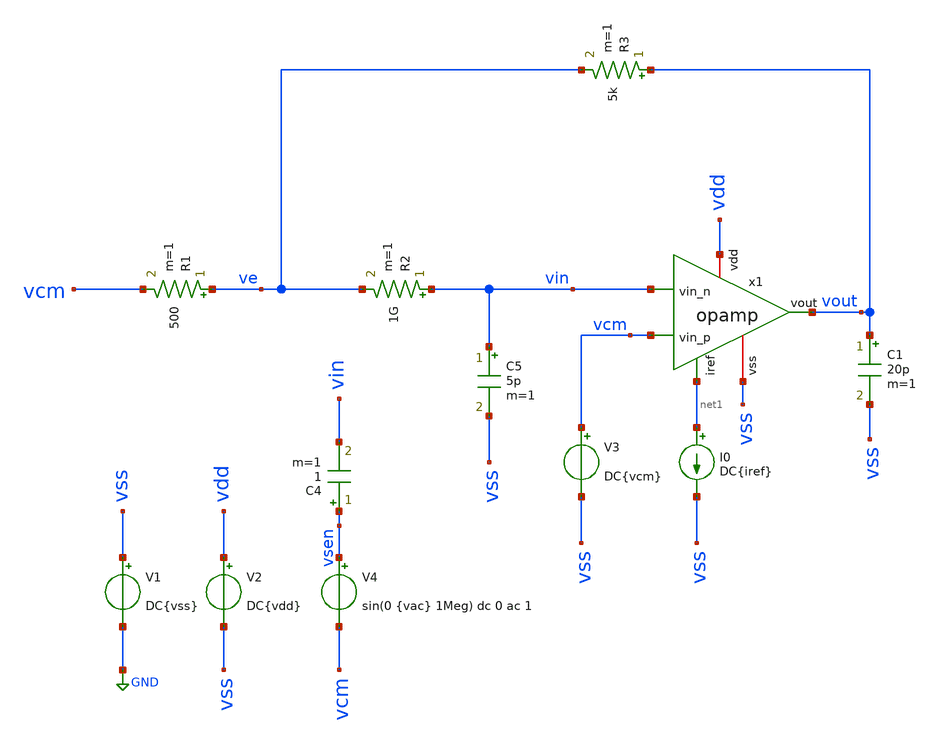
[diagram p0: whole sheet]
** sch_path: xsch/sch/opamp/opamp_openloop.sch
**.subckt opamp_openloop
V1 vss GND DC{vss}
V2 vdd vss DC{vdd}
V3 vcm vss DC{vcm}
V4 vsen vcm sin(0 {vac} 1Meg) dc 0 ac 1
C4 vsen vin 1 m=1
I0 net1 vss DC{iref}
R1 ve vcm 500 m=1
R2 vin ve 1G m=1
R3 vout ve 5k m=1
C5 vin vss 5p m=1
C1 vout vss 20p m=1
x1 vdd net1 vin vcm vout vss opamp
**** begin user architecture code




* Circuit Parameters
.param iref = 100u
.param vdd  = 1.8
.param vss  = 0.0
.param vcm  = 0.8
.param vac  = 10m
.options TEMP = 65.0

* Include Models
.lib /home/tools/repos_sky130/skywater-pdk/libraries/sky130_fd_pr_ngspice/latest/models/corners/sky130.lib FS

* OP Parameters & Singals to save
.save all  @M.X1.XM1.msky130_fd_pr__pfet_01v8[id] @M.X1.XM1.msky130_fd_pr__pfet_01v8[vth] @M.X1.XM1.msky130_fd_pr__pfet_01v8[vgs] @M.X1.XM1.msky130_fd_pr__pfet_01v8[vds] @M.X1.XM1.msky130_fd_pr__pfet_01v8[vdsat] @M.X1.XM1.msky130_fd_pr__pfet_01v8[gm] @M.X1.XM1.msky130_fd_pr__pfet_01v8[gds]  @M.X1.XM2.msky130_fd_pr__pfet_01v8[id] @M.X1.XM2.msky130_fd_pr__pfet_01v8[vth] @M.X1.XM2.msky130_fd_pr__pfet_01v8[vgs] @M.X1.XM2.msky130_fd_pr__pfet_01v8[vds] @M.X1.XM2.msky130_fd_pr__pfet_01v8[vdsat] @M.X1.XM2.msky130_fd_pr__pfet_01v8[gm] @M.X1.XM2.msky130_fd_pr__pfet_01v8[gds]  @M.X1.XM3.msky130_fd_pr__nfet_01v8[id] @M.X1.XM3.msky130_fd_pr__nfet_01v8[vth] @M.X1.XM3.msky130_fd_pr__nfet_01v8[vgs] @M.X1.XM3.msky130_fd_pr__nfet_01v8[vds] @M.X1.XM3.msky130_fd_pr__nfet_01v8[vdsat] @M.X1.XM3.msky130_fd_pr__nfet_01v8[gm] @M.X1.XM3.msky130_fd_pr__nfet_01v8[gds]  @M.X1.XM4.msky130_fd_pr__nfet_01v8[id] @M.X1.XM4.msky130_fd_pr__nfet_01v8[vth] @M.X1.XM4.msky130_fd_pr__nfet_01v8[vgs] @M.X1.XM4.msky130_fd_pr__nfet_01v8[vds] @M.X1.XM4.msky130_fd_pr__nfet_01v8[vdsat] @M.X1.XM4.msky130_fd_pr__nfet_01v8[gm] @M.X1.XM4.msky130_fd_pr__nfet_01v8[gds]  @M.X1.XM5.msky130_fd_pr__pfet_01v8[id] @M.X1.XM5.msky130_fd_pr__pfet_01v8[vth] @M.X1.XM5.msky130_fd_pr__pfet_01v8[vgs] @M.X1.XM5.msky130_fd_pr__pfet_01v8[vds] @M.X1.XM5.msky130_fd_pr__pfet_01v8[vdsat] @M.X1.XM5.msky130_fd_pr__pfet_01v8[gm] @M.X1.XM5.msky130_fd_pr__pfet_01v8[gds]  @M.X1.XM6.msky130_fd_pr__nfet_01v8[id] @M.X1.XM6.msky130_fd_pr__nfet_01v8[vth] @M.X1.XM6.msky130_fd_pr__nfet_01v8[vgs] @M.X1.XM6.msky130_fd_pr__nfet_01v8[vds] @M.X1.XM6.msky130_fd_pr__nfet_01v8[vdsat] @M.X1.XM6.msky130_fd_pr__nfet_01v8[gm] @M.X1.XM6.msky130_fd_pr__nfet_01v8[gds]  @M.X1.XM7.msky130_fd_pr__pfet_01v8[id] @M.X1.XM7.msky130_fd_pr__pfet_01v8[vth] @M.X1.XM7.msky130_fd_pr__pfet_01v8[vgs] @M.X1.XM7.msky130_fd_pr__pfet_01v8[vds] @M.X1.XM7.msky130_fd_pr__pfet_01v8[vdsat] @M.X1.XM7.msky130_fd_pr__pfet_01v8[gm] @M.X1.XM7.msky130_fd_pr__pfet_01v8[gds]  @M.X1.XM8.msky130_fd_pr__pfet_01v8[id] @M.X1.XM8.msky130_fd_pr__pfet_01v8[vth] @M.X1.XM8.msky130_fd_pr__pfet_01v8[vgs] @M.X1.XM8.msky130_fd_pr__pfet_01v8[vds] @M.X1.XM8.msky130_fd_pr__pfet_01v8[vdsat] @M.X1.XM8.msky130_fd_pr__pfet_01v8[gm] @M.X1.XM8.msky130_fd_pr__pfet_01v8[gds]  @M.X1.XM9.msky130_fd_pr__nfet_01v8[id] @M.X1.XM9.msky130_fd_pr__nfet_01v8[vth] @M.X1.XM9.msky130_fd_pr__nfet_01v8[vgs] @M.X1.XM9.msky130_fd_pr__nfet_01v8[vds] @M.X1.XM9.msky130_fd_pr__nfet_01v8[vdsat] @M.X1.XM9.msky130_fd_pr__nfet_01v8[gm] @M.X1.XM9.msky130_fd_pr__nfet_01v8[gds]

*Simulation
.control

  *ac dec 100 1 10G
  *setplot ac1
  *meas ac GBW when vdb(vout)=0
  *meas ac DCG find vdb(vout) at=1
  *meas ac PM find vp(vout) when vdb(vout)=0
  *print PM*180/PI
  *meas ac GM find vdb(vout) when vp(vout)=0
  *plot vdb(vout) {vp(vout)*180/PI}
  *write ~/whiteboard_sky130/xsch/results_sch/opamp/opamp_openloop_ac1.raw

  *reset
  op
  save all
  *setplot op1
  write ~/whiteboard_sky130/xsch/results_sch/opamp/opamp_openloop_op.raw
  *write opamp_openloop.raw

.endc

.end


**** end user architecture code
**.ends

* expanding   symbol:  opamp.sym # of pins=6
** sym_path: opamp.sym
** sch_path: opamp.sch
.subckt opamp vdd iref vin_n vin_p vout vss
*.iopin vdd
*.iopin vss
*.ipin vin_n
*.ipin vin_p
*.ipin iref
*.opin vout
XM1 vbn vin_n vp vp sky130_fd_pr__pfet_01v8 L=0.3 W=3 nf=1 ad='W * 0.29' as='W * 0.29' pd='2 * (W + 0.29)'
+ ps='2 * (W + 0.29)' nrd='0.29 / W' nrs='0.29 / W' sa=0 sb=0 sd=0 mult=200 m=200
XM2 voe1 vin_p vp vp sky130_fd_pr__pfet_01v8 L=0.3 W=3 nf=1 ad='W * 0.29' as='W * 0.29' pd='2 * (W + 0.29)'
+ ps='2 * (W + 0.29)' nrd='0.29 / W' nrs='0.29 / W' sa=0 sb=0 sd=0 mult=200 m=200
XM3 vbn vbn vss vss sky130_fd_pr__nfet_01v8 L=0.3 W=3 nf=1 ad='W * 0.29' as='W * 0.29' pd='2 * (W + 0.29)'
+ ps='2 * (W + 0.29)' nrd='0.29 / W' nrs='0.29 / W' sa=0 sb=0 sd=0 mult=30 m=30
XM4 voe1 vbn vss vss sky130_fd_pr__nfet_01v8 L=0.3 W=3 nf=1 ad='W * 0.29' as='W * 0.29' pd='2 * (W + 0.29)'
+ ps='2 * (W + 0.29)' nrd='0.29 / W' nrs='0.29 / W' sa=0 sb=0 sd=0 mult=30 m=30
XM5 vp iref vdd vdd sky130_fd_pr__pfet_01v8 L=0.3 W=3 nf=1 ad='W * 0.29' as='W * 0.29' pd='2 * (W + 0.29)'
+ ps='2 * (W + 0.29)' nrd='0.29 / W' nrs='0.29 / W' sa=0 sb=0 sd=0 mult=30 m=30
XM7 vout iref vdd vdd sky130_fd_pr__pfet_01v8 L=0.3 W=3 nf=1 ad='W * 0.29' as='W * 0.29' pd='2 * (W + 0.29)'
+ ps='2 * (W + 0.29)' nrd='0.29 / W' nrs='0.29 / W' sa=0 sb=0 sd=0 mult=150 m=150
XM8 iref iref vdd vdd sky130_fd_pr__pfet_01v8 L=0.3 W=3 nf=1 ad='W * 0.29' as='W * 0.29' pd='2 * (W + 0.29)'
+ ps='2 * (W + 0.29)' nrd='0.29 / W' nrs='0.29 / W' sa=0 sb=0 sd=0 mult=15 m=15
XM9 net1 vdd voe1 vss sky130_fd_pr__nfet_01v8 L=0.15 W=0.75 nf=1 ad='W * 0.29' as='W * 0.29' pd='2 * (W + 0.29)'
+ ps='2 * (W + 0.29)' nrd='0.29 / W' nrs='0.29 / W' sa=0 sb=0 sd=0 mult=6 m=6
XC1 net1 vout sky130_fd_pr__cap_mim_m3_1 W=17.55 L=15 MF=6 m=6
XM6 vout voe1 vss vss sky130_fd_pr__nfet_01v8 L=0.45 W=4.5 nf=1 ad='W * 0.29' as='W * 0.29' pd='2 * (W + 0.29)'
+ ps='2 * (W + 0.29)' nrd='0.29 / W' nrs='0.29 / W' sa=0 sb=0 sd=0 mult=150 m=150
.ends

.GLOBAL GND
.end
